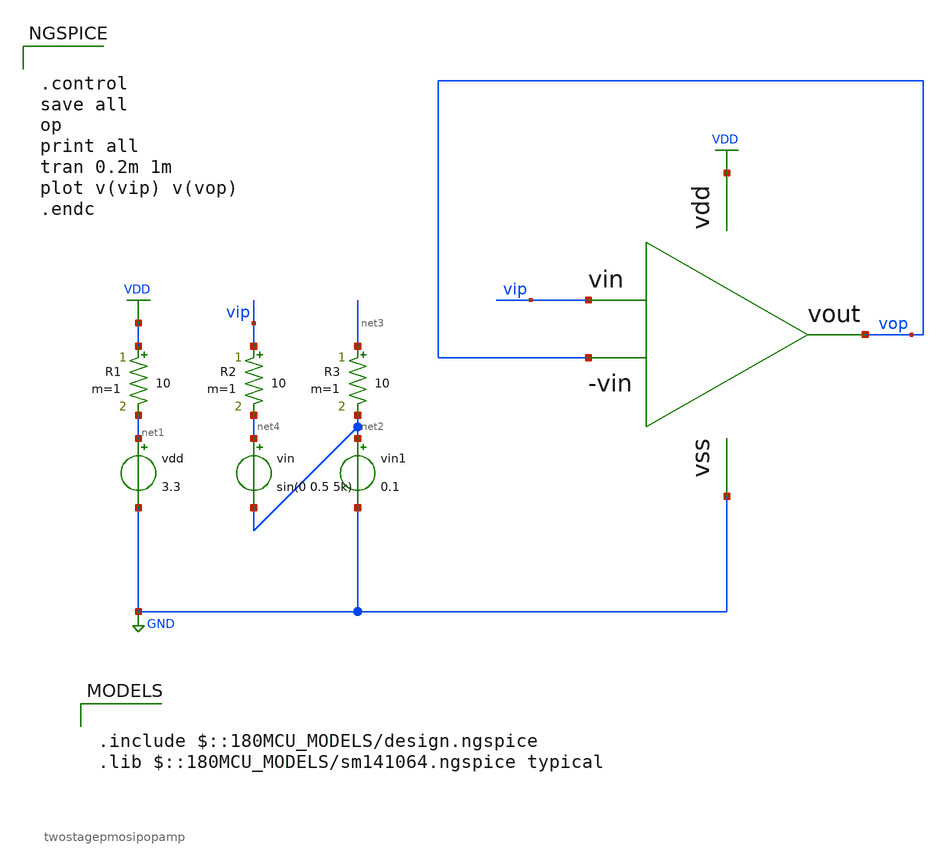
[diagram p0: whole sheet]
** sch_path: designs/First cut design/2stage_nmos_opamp_tb.sch
**.subckt 2stage_nmos_opamp_tb
vin net4 net2 sin(0 0.5 5k)
vin1 net2 GND 0.1
vdd net1 GND 3.3
xOTA1 vip VDD vop vop GND twostagepmosipopamp
R1 VDD net1 10 m=1
R2 vip net4 10 m=1
R3 net3 net2 10 m=1
**** begin user architecture code


.control
save all
op
print all
tran 0.2m 1m
plot v(vip) v(vop)
.endc


.include $::180MCU_MODELS/design.ngspice
.lib $::180MCU_MODELS/sm141064.ngspice typical

**** end user architecture code
**.ends
.GLOBAL GND
.GLOBAL VDD
.end
